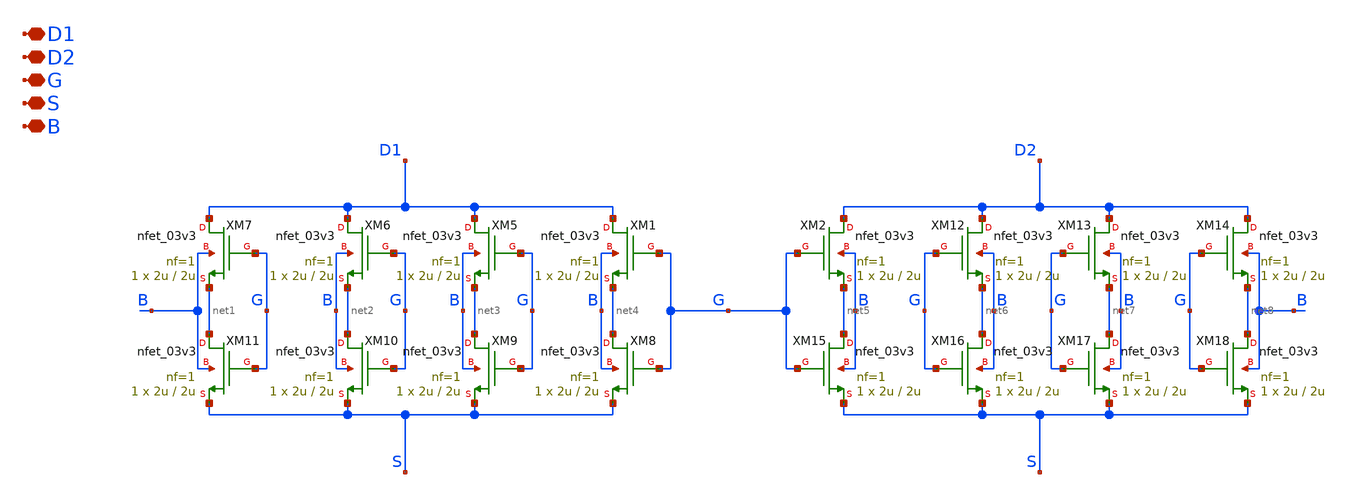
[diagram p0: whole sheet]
** sch_path: TIA_Filter/PseudoResistor/DiffP_nfets.sch
**.subckt DiffP_nfets D1 D2 G S B
*.iopin D1
*.iopin D2
*.iopin G
*.iopin S
*.iopin B
XM1 D1 G net4 B nfet_03v3 L=2u W=2u nf=1 ad='int((nf+1)/2) * W/nf * 0.18u' as='int((nf+2)/2) * W/nf * 0.18u'
+ pd='2*int((nf+1)/2) * (W/nf + 0.18u)' ps='2*int((nf+2)/2) * (W/nf + 0.18u)' nrd='0.18u / W' nrs='0.18u / W'
+ sa=0 sb=0 sd=0 m=1
XM2 D2 G net5 B nfet_03v3 L=2u W=2u nf=1 ad='int((nf+1)/2) * W/nf * 0.18u' as='int((nf+2)/2) * W/nf * 0.18u'
+ pd='2*int((nf+1)/2) * (W/nf + 0.18u)' ps='2*int((nf+2)/2) * (W/nf + 0.18u)' nrd='0.18u / W' nrs='0.18u / W'
+ sa=0 sb=0 sd=0 m=1
XM5 D1 G net3 B nfet_03v3 L=2u W=2u nf=1 ad='int((nf+1)/2) * W/nf * 0.18u' as='int((nf+2)/2) * W/nf * 0.18u'
+ pd='2*int((nf+1)/2) * (W/nf + 0.18u)' ps='2*int((nf+2)/2) * (W/nf + 0.18u)' nrd='0.18u / W' nrs='0.18u / W'
+ sa=0 sb=0 sd=0 m=1
XM6 D1 G net2 B nfet_03v3 L=2u W=2u nf=1 ad='int((nf+1)/2) * W/nf * 0.18u' as='int((nf+2)/2) * W/nf * 0.18u'
+ pd='2*int((nf+1)/2) * (W/nf + 0.18u)' ps='2*int((nf+2)/2) * (W/nf + 0.18u)' nrd='0.18u / W' nrs='0.18u / W'
+ sa=0 sb=0 sd=0 m=1
XM7 D1 G net1 B nfet_03v3 L=2u W=2u nf=1 ad='int((nf+1)/2) * W/nf * 0.18u' as='int((nf+2)/2) * W/nf * 0.18u'
+ pd='2*int((nf+1)/2) * (W/nf + 0.18u)' ps='2*int((nf+2)/2) * (W/nf + 0.18u)' nrd='0.18u / W' nrs='0.18u / W'
+ sa=0 sb=0 sd=0 m=1
XM8 net4 G S B nfet_03v3 L=2u W=2u nf=1 ad='int((nf+1)/2) * W/nf * 0.18u' as='int((nf+2)/2) * W/nf * 0.18u'
+ pd='2*int((nf+1)/2) * (W/nf + 0.18u)' ps='2*int((nf+2)/2) * (W/nf + 0.18u)' nrd='0.18u / W' nrs='0.18u / W'
+ sa=0 sb=0 sd=0 m=1
XM9 net3 G S B nfet_03v3 L=2u W=2u nf=1 ad='int((nf+1)/2) * W/nf * 0.18u' as='int((nf+2)/2) * W/nf * 0.18u'
+ pd='2*int((nf+1)/2) * (W/nf + 0.18u)' ps='2*int((nf+2)/2) * (W/nf + 0.18u)' nrd='0.18u / W' nrs='0.18u / W'
+ sa=0 sb=0 sd=0 m=1
XM10 net2 G S B nfet_03v3 L=2u W=2u nf=1 ad='int((nf+1)/2) * W/nf * 0.18u' as='int((nf+2)/2) * W/nf * 0.18u'
+ pd='2*int((nf+1)/2) * (W/nf + 0.18u)' ps='2*int((nf+2)/2) * (W/nf + 0.18u)' nrd='0.18u / W' nrs='0.18u / W'
+ sa=0 sb=0 sd=0 m=1
XM11 net1 G S B nfet_03v3 L=2u W=2u nf=1 ad='int((nf+1)/2) * W/nf * 0.18u' as='int((nf+2)/2) * W/nf * 0.18u'
+ pd='2*int((nf+1)/2) * (W/nf + 0.18u)' ps='2*int((nf+2)/2) * (W/nf + 0.18u)' nrd='0.18u / W' nrs='0.18u / W'
+ sa=0 sb=0 sd=0 m=1
XM12 D2 G net6 B nfet_03v3 L=2u W=2u nf=1 ad='int((nf+1)/2) * W/nf * 0.18u' as='int((nf+2)/2) * W/nf * 0.18u'
+ pd='2*int((nf+1)/2) * (W/nf + 0.18u)' ps='2*int((nf+2)/2) * (W/nf + 0.18u)' nrd='0.18u / W' nrs='0.18u / W'
+ sa=0 sb=0 sd=0 m=1
XM13 D2 G net7 B nfet_03v3 L=2u W=2u nf=1 ad='int((nf+1)/2) * W/nf * 0.18u' as='int((nf+2)/2) * W/nf * 0.18u'
+ pd='2*int((nf+1)/2) * (W/nf + 0.18u)' ps='2*int((nf+2)/2) * (W/nf + 0.18u)' nrd='0.18u / W' nrs='0.18u / W'
+ sa=0 sb=0 sd=0 m=1
XM14 D2 G net8 B nfet_03v3 L=2u W=2u nf=1 ad='int((nf+1)/2) * W/nf * 0.18u' as='int((nf+2)/2) * W/nf * 0.18u'
+ pd='2*int((nf+1)/2) * (W/nf + 0.18u)' ps='2*int((nf+2)/2) * (W/nf + 0.18u)' nrd='0.18u / W' nrs='0.18u / W'
+ sa=0 sb=0 sd=0 m=1
XM15 net5 G S B nfet_03v3 L=2u W=2u nf=1 ad='int((nf+1)/2) * W/nf * 0.18u' as='int((nf+2)/2) * W/nf * 0.18u'
+ pd='2*int((nf+1)/2) * (W/nf + 0.18u)' ps='2*int((nf+2)/2) * (W/nf + 0.18u)' nrd='0.18u / W' nrs='0.18u / W'
+ sa=0 sb=0 sd=0 m=1
XM16 net6 G S B nfet_03v3 L=2u W=2u nf=1 ad='int((nf+1)/2) * W/nf * 0.18u' as='int((nf+2)/2) * W/nf * 0.18u'
+ pd='2*int((nf+1)/2) * (W/nf + 0.18u)' ps='2*int((nf+2)/2) * (W/nf + 0.18u)' nrd='0.18u / W' nrs='0.18u / W'
+ sa=0 sb=0 sd=0 m=1
XM17 net7 G S B nfet_03v3 L=2u W=2u nf=1 ad='int((nf+1)/2) * W/nf * 0.18u' as='int((nf+2)/2) * W/nf * 0.18u'
+ pd='2*int((nf+1)/2) * (W/nf + 0.18u)' ps='2*int((nf+2)/2) * (W/nf + 0.18u)' nrd='0.18u / W' nrs='0.18u / W'
+ sa=0 sb=0 sd=0 m=1
XM18 net8 G S B nfet_03v3 L=2u W=2u nf=1 ad='int((nf+1)/2) * W/nf * 0.18u' as='int((nf+2)/2) * W/nf * 0.18u'
+ pd='2*int((nf+1)/2) * (W/nf + 0.18u)' ps='2*int((nf+2)/2) * (W/nf + 0.18u)' nrd='0.18u / W' nrs='0.18u / W'
+ sa=0 sb=0 sd=0 m=1
**.ends
.end
